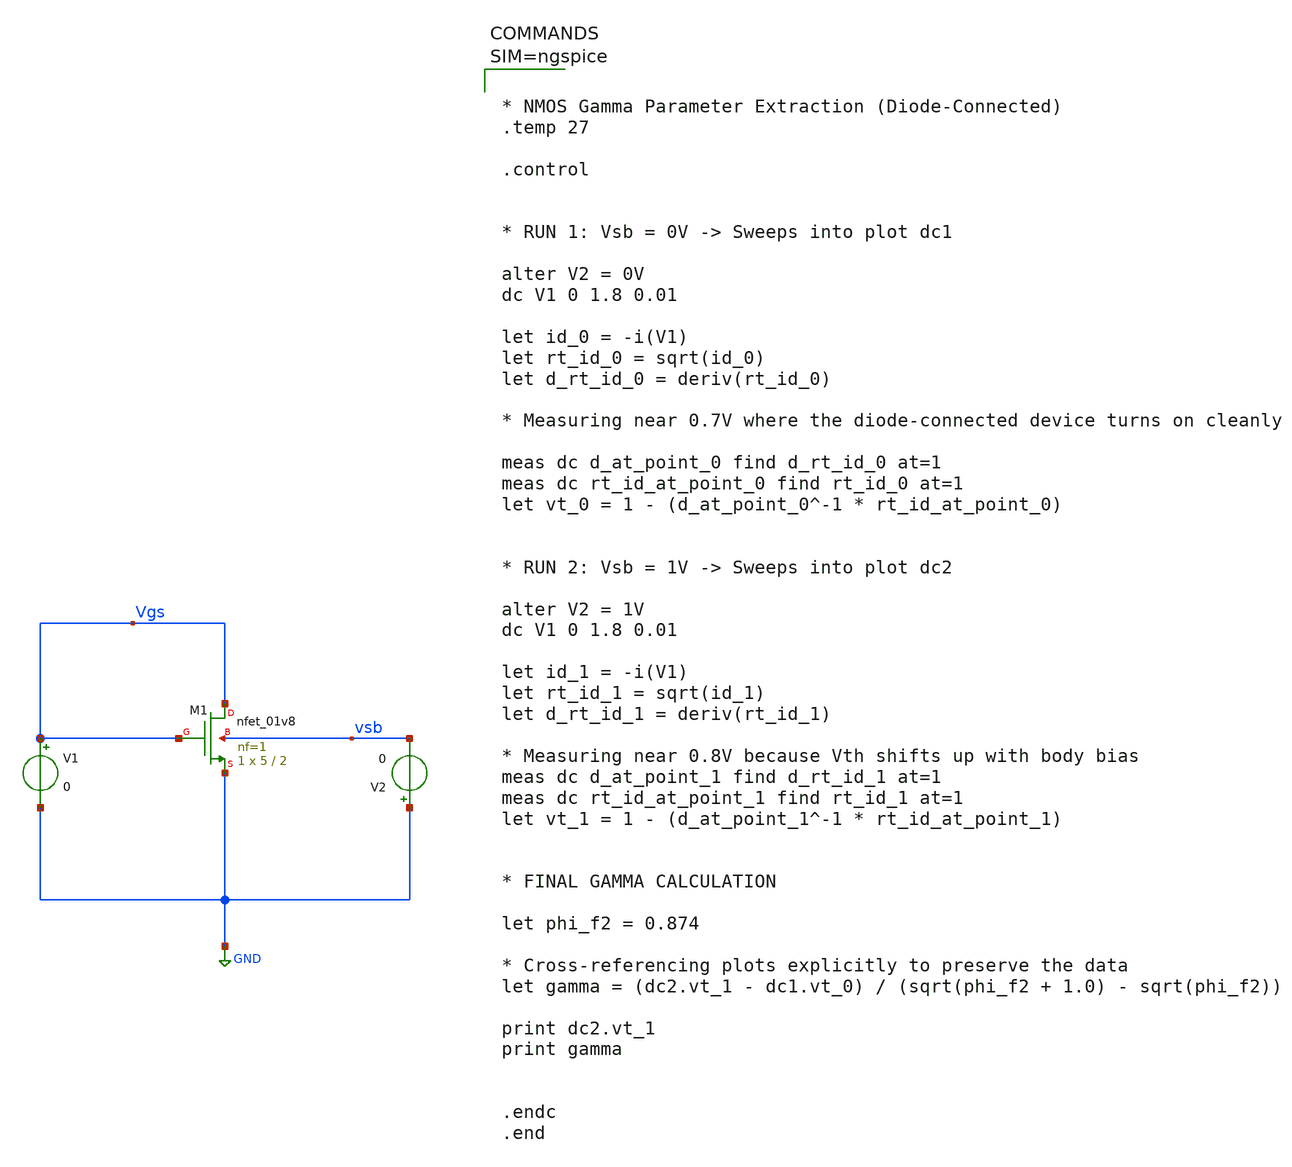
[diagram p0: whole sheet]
** sch_path: testbenches/NMOS_gamma.sch
**.subckt NMOS_gamma
XM1 Vgs Vgs GND vsb sky130_fd_pr__nfet_01v8 L=2 W=5 nf=1 ad='int((1 + 1)/2) * 5 / 1 * 0.29' as='int((1 + 2)/2) * 5 / 1 * 0.29'
+ pd='2*int((1 + 1)/2) * (5 / 1 + 0.29)' ps='2*int((1 + 2)/2) * (5 / 1 + 0.29)' nrd='0.29 / 5 ' nrs='0.29 / 5 '
+ sa=0 sb=0 sd=0 mult=1 m=1
V1 Vgs GND 0
V2 GND vsb 0
**** begin user architecture code

** opencircuitdesign pdks install
.lib $::SKYWATER_MODELS/sky130.lib.spice tt




* NMOS Gamma Parameter Extraction (Diode-Connected)
.temp 27

.control


* RUN 1: Vsb = 0V -> Sweeps into plot dc1

alter V2 = 0V
dc V1 0 1.8 0.01

let id_0 = -i(V1)
let rt_id_0 = sqrt(id_0)
let d_rt_id_0 = deriv(rt_id_0)

* Measuring near 0.7V where the diode-connected device turns on cleanly

meas dc d_at_point_0 find d_rt_id_0 at=1
meas dc rt_id_at_point_0 find rt_id_0 at=1
let vt_0 = 1 - (d_at_point_0^-1 * rt_id_at_point_0)


* RUN 2: Vsb = 1V -> Sweeps into plot dc2

alter V2 = 1V
dc V1 0 1.8 0.01

let id_1 = -i(V1)
let rt_id_1 = sqrt(id_1)
let d_rt_id_1 = deriv(rt_id_1)

* Measuring near 0.8V because Vth shifts up with body bias
meas dc d_at_point_1 find d_rt_id_1 at=1
meas dc rt_id_at_point_1 find rt_id_1 at=1
let vt_1 = 1 - (d_at_point_1^-1 * rt_id_at_point_1)


* FINAL GAMMA CALCULATION

let phi_f2 = 0.874

* Cross-referencing plots explicitly to preserve the data
let gamma = (dc2.vt_1 - dc1.vt_0) / (sqrt(phi_f2 + 1.0) - sqrt(phi_f2))

print dc2.vt_1
print gamma


.endc
.end



**** end user architecture code
**.ends
.GLOBAL GND
.end
